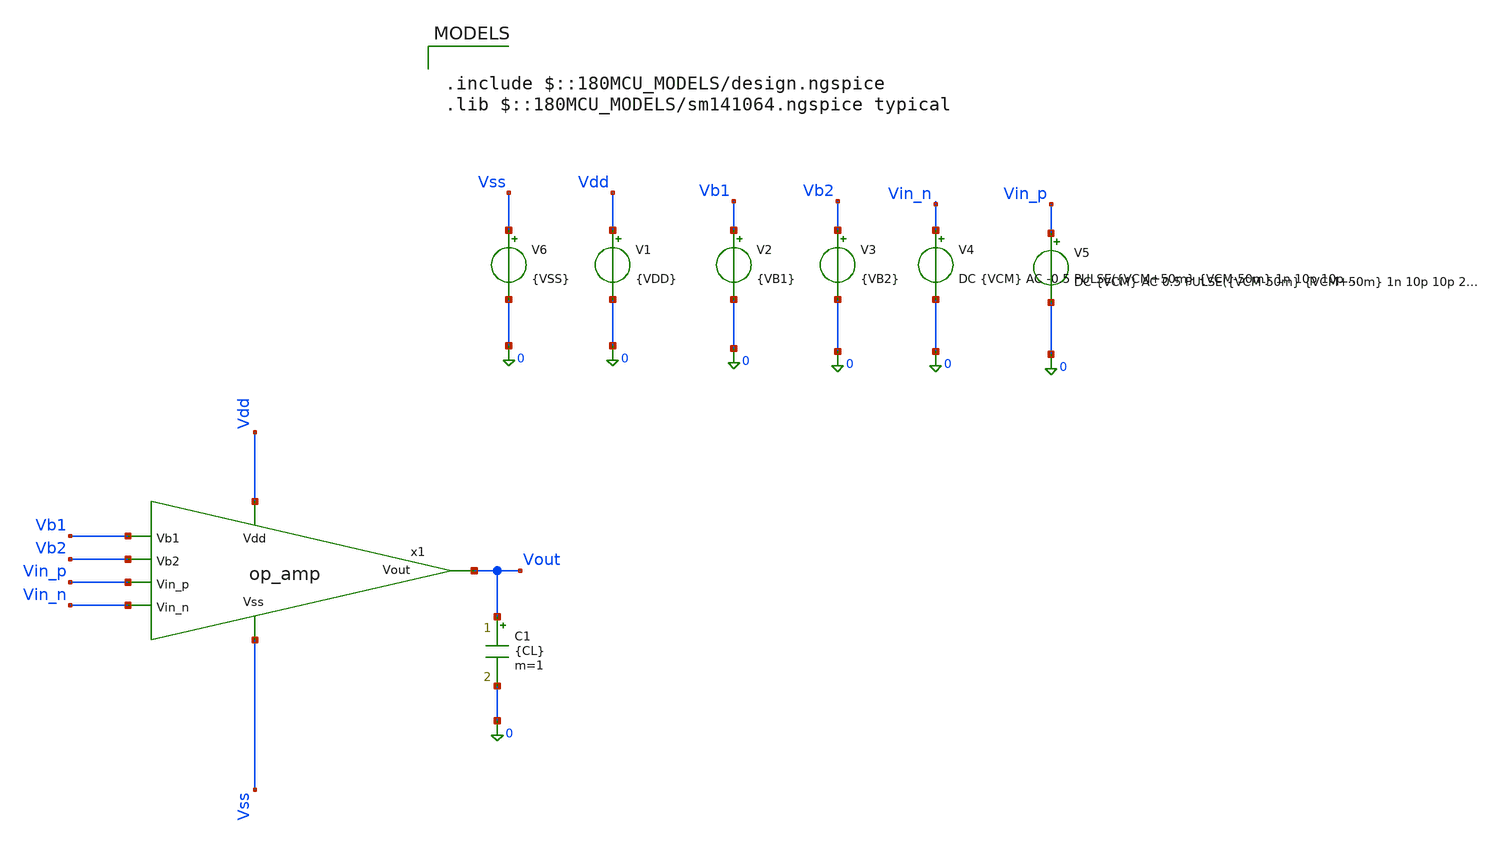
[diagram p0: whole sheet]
** sch_path: blocks/adc/lvds/ota_performance_test.sch
**.subckt ota_performance_test
x1 Vdd Vb1 Vout Vb2 Vin_p Vin_n Vss op_amp
V1 Vdd 0 {VDD}
V2 Vb1 0 {VB1}
V3 Vb2 0 {VB2}
V4 Vin_n 0 DC {VCM} AC -0.5 PULSE({VCM+50m} {VCM-50m} 1n 10p 10p 20n 50n)
V5 Vin_p 0 DC {VCM} AC 0.5 PULSE({VCM-50m} {VCM+50m} 1n 10p 10p 20n 50n)
V6 Vss 0 {VSS}
C1 Vout 0 {CL} m=1
**** begin user architecture code


.param VDD=3.3
.param VSS=0
.param VCM=1.2
.param VB1=0.0
.param VB2=1.5
.param IB=100u
.param CL=10f

.control
save all
set filetype=ascii
set wr_singlescale
set wr_vecnames

op

* AC gain
ac dec 50 1 100G
let vin_diff_ac = v(Vin_p)-v(Vin_n)
let gain = v(Vout)/vin_diff_ac
wrdata /foss/designs/trans_testing/ota_testing/ota_ac.txt frequency mag(gain) db(gain) ph(gain)

* Transient slew rate
tran 1p 50n
let vin_diff = v(Vin_p)-v(Vin_n)
let slew = deriv(v(Vout))
wrdata /foss/designs/trans_testing/ota_testing/ota_tran.txt time v(Vin_p) v(Vin_n) vin_diff v(Vout)
+ slew

.endc



.include $::180MCU_MODELS/design.ngspice
.lib $::180MCU_MODELS/sm141064.ngspice typical

**** end user architecture code
**.ends

* expanding   symbol:  op_amp.sym # of pins=7
** sym_path: blocks/adc/lvds/op_amp.sym
** sch_path: blocks/adc/lvds/op_amp.sch
.subckt op_amp Vdd Vb1 Vout Vb2 Vin_p Vin_n Vss
*.ipin Vdd
*.ipin Vb2
*.ipin Vin_p
*.ipin Vin_n
*.ipin Vb1
*.opin Vout
*.ipin Vss
XM1 VdM1 vgM1 Vdd Vdd pfet_03v3 L=0.28u W=10.5u nf=1 ad='int((nf+1)/2) * W/nf * 0.18u' as='int((nf+2)/2) * W/nf * 0.18u'
+ pd='2*int((nf+1)/2) * (W/nf + 0.18u)' ps='2*int((nf+2)/2) * (W/nf + 0.18u)' nrd='0.18u / W' nrs='0.18u / W'
+ sa=0 sb=0 sd=0 m=1
XM2 VdM2 VdM4 Vdd Vdd pfet_03v3 L=0.28u W=10.5u nf=1 ad='int((nf+1)/2) * W/nf * 0.18u' as='int((nf+2)/2) * W/nf * 0.18u'
+ pd='2*int((nf+1)/2) * (W/nf + 0.18u)' ps='2*int((nf+2)/2) * (W/nf + 0.18u)' nrd='0.18u / W' nrs='0.18u / W'
+ sa=0 sb=0 sd=0 m=1
XM3 vgM1 Vb2 VdM1 Vdd pfet_03v3 L=0.28u W=10.5u nf=1 ad='int((nf+1)/2) * W/nf * 0.18u' as='int((nf+2)/2) * W/nf * 0.18u'
+ pd='2*int((nf+1)/2) * (W/nf + 0.18u)' ps='2*int((nf+2)/2) * (W/nf + 0.18u)' nrd='0.18u / W' nrs='0.18u / W'
+ sa=0 sb=0 sd=0 m=1
XM4 VdM4 Vb2 VdM2 Vdd pfet_03v3 L=0.28u W=10.5u nf=1 ad='int((nf+1)/2) * W/nf * 0.18u' as='int((nf+2)/2) * W/nf * 0.18u'
+ pd='2*int((nf+1)/2) * (W/nf + 0.18u)' ps='2*int((nf+2)/2) * (W/nf + 0.18u)' nrd='0.18u / W' nrs='0.18u / W'
+ sa=0 sb=0 sd=0 m=1
XM5 VdM4 Vin_p net1 Vss nfet_03v3 L=0.28u W=52.5u nf=15 ad='int((nf+1)/2) * W/nf * 0.18u' as='int((nf+2)/2) * W/nf * 0.18u'
+ pd='2*int((nf+1)/2) * (W/nf + 0.18u)' ps='2*int((nf+2)/2) * (W/nf + 0.18u)' nrd='0.18u / W' nrs='0.18u / W'
+ sa=0 sb=0 sd=0 m=1
XM6 vgM1 Vin_n net1 Vss nfet_03v3 L=0.28u W=52.5u nf=15 ad='int((nf+1)/2) * W/nf * 0.18u' as='int((nf+2)/2) * W/nf * 0.18u'
+ pd='2*int((nf+1)/2) * (W/nf + 0.18u)' ps='2*int((nf+2)/2) * (W/nf + 0.18u)' nrd='0.18u / W' nrs='0.18u / W'
+ sa=0 sb=0 sd=0 m=1
XM7 VdM7 VdM4 Vdd Vdd pfet_03v3 L=0.28u W=10.5u nf=1 ad='int((nf+1)/2) * W/nf * 0.18u' as='int((nf+2)/2) * W/nf * 0.18u'
+ pd='2*int((nf+1)/2) * (W/nf + 0.18u)' ps='2*int((nf+2)/2) * (W/nf + 0.18u)' nrd='0.18u / W' nrs='0.18u / W'
+ sa=0 sb=0 sd=0 m=1
XM9 VdM9 vgM1 Vdd Vdd pfet_03v3 L=0.28u W=10.5u nf=1 ad='int((nf+1)/2) * W/nf * 0.18u' as='int((nf+2)/2) * W/nf * 0.18u'
+ pd='2*int((nf+1)/2) * (W/nf + 0.18u)' ps='2*int((nf+2)/2) * (W/nf + 0.18u)' nrd='0.18u / W' nrs='0.18u / W'
+ sa=0 sb=0 sd=0 m=1
XM11 VgM14 Vb2 net3 Vss nfet_03v3 L=0.28u W=5.25u nf=1 ad='int((nf+1)/2) * W/nf * 0.18u' as='int((nf+2)/2) * W/nf * 0.18u'
+ pd='2*int((nf+1)/2) * (W/nf + 0.18u)' ps='2*int((nf+2)/2) * (W/nf + 0.18u)' nrd='0.18u / W' nrs='0.18u / W'
+ sa=0 sb=0 sd=0 m=1
XM12 Vout Vb2 net2 Vss nfet_03v3 L=0.28u W=5.25u nf=1 ad='int((nf+1)/2) * W/nf * 0.18u' as='int((nf+2)/2) * W/nf * 0.18u'
+ pd='2*int((nf+1)/2) * (W/nf + 0.18u)' ps='2*int((nf+2)/2) * (W/nf + 0.18u)' nrd='0.18u / W' nrs='0.18u / W'
+ sa=0 sb=0 sd=0 m=1
XM13 net3 VgM14 0 Vss nfet_03v3 L=0.28u W=5.25u nf=1 ad='int((nf+1)/2) * W/nf * 0.18u' as='int((nf+2)/2) * W/nf * 0.18u'
+ pd='2*int((nf+1)/2) * (W/nf + 0.18u)' ps='2*int((nf+2)/2) * (W/nf + 0.18u)' nrd='0.18u / W' nrs='0.18u / W'
+ sa=0 sb=0 sd=0 m=1
XM14 net2 VgM14 0 Vss nfet_03v3 L=0.28u W=5.25u nf=1 ad='int((nf+1)/2) * W/nf * 0.18u' as='int((nf+2)/2) * W/nf * 0.18u'
+ pd='2*int((nf+1)/2) * (W/nf + 0.18u)' ps='2*int((nf+2)/2) * (W/nf + 0.18u)' nrd='0.18u / W' nrs='0.18u / W'
+ sa=0 sb=0 sd=0 m=1
XM8 VgM14 Vb1 VdM7 Vdd pfet_03v3 L=0.28u W=10.5u nf=1 ad='int((nf+1)/2) * W/nf * 0.18u' as='int((nf+2)/2) * W/nf * 0.18u'
+ pd='2*int((nf+1)/2) * (W/nf + 0.18u)' ps='2*int((nf+2)/2) * (W/nf + 0.18u)' nrd='0.18u / W' nrs='0.18u / W'
+ sa=0 sb=0 sd=0 m=1
XM10 Vout Vb1 VdM9 Vdd pfet_03v3 L=0.28u W=10.5u nf=1 ad='int((nf+1)/2) * W/nf * 0.18u' as='int((nf+2)/2) * W/nf * 0.18u'
+ pd='2*int((nf+1)/2) * (W/nf + 0.18u)' ps='2*int((nf+2)/2) * (W/nf + 0.18u)' nrd='0.18u / W' nrs='0.18u / W'
+ sa=0 sb=0 sd=0 m=1
ibias net1 Vss 300u
.ends

.end
